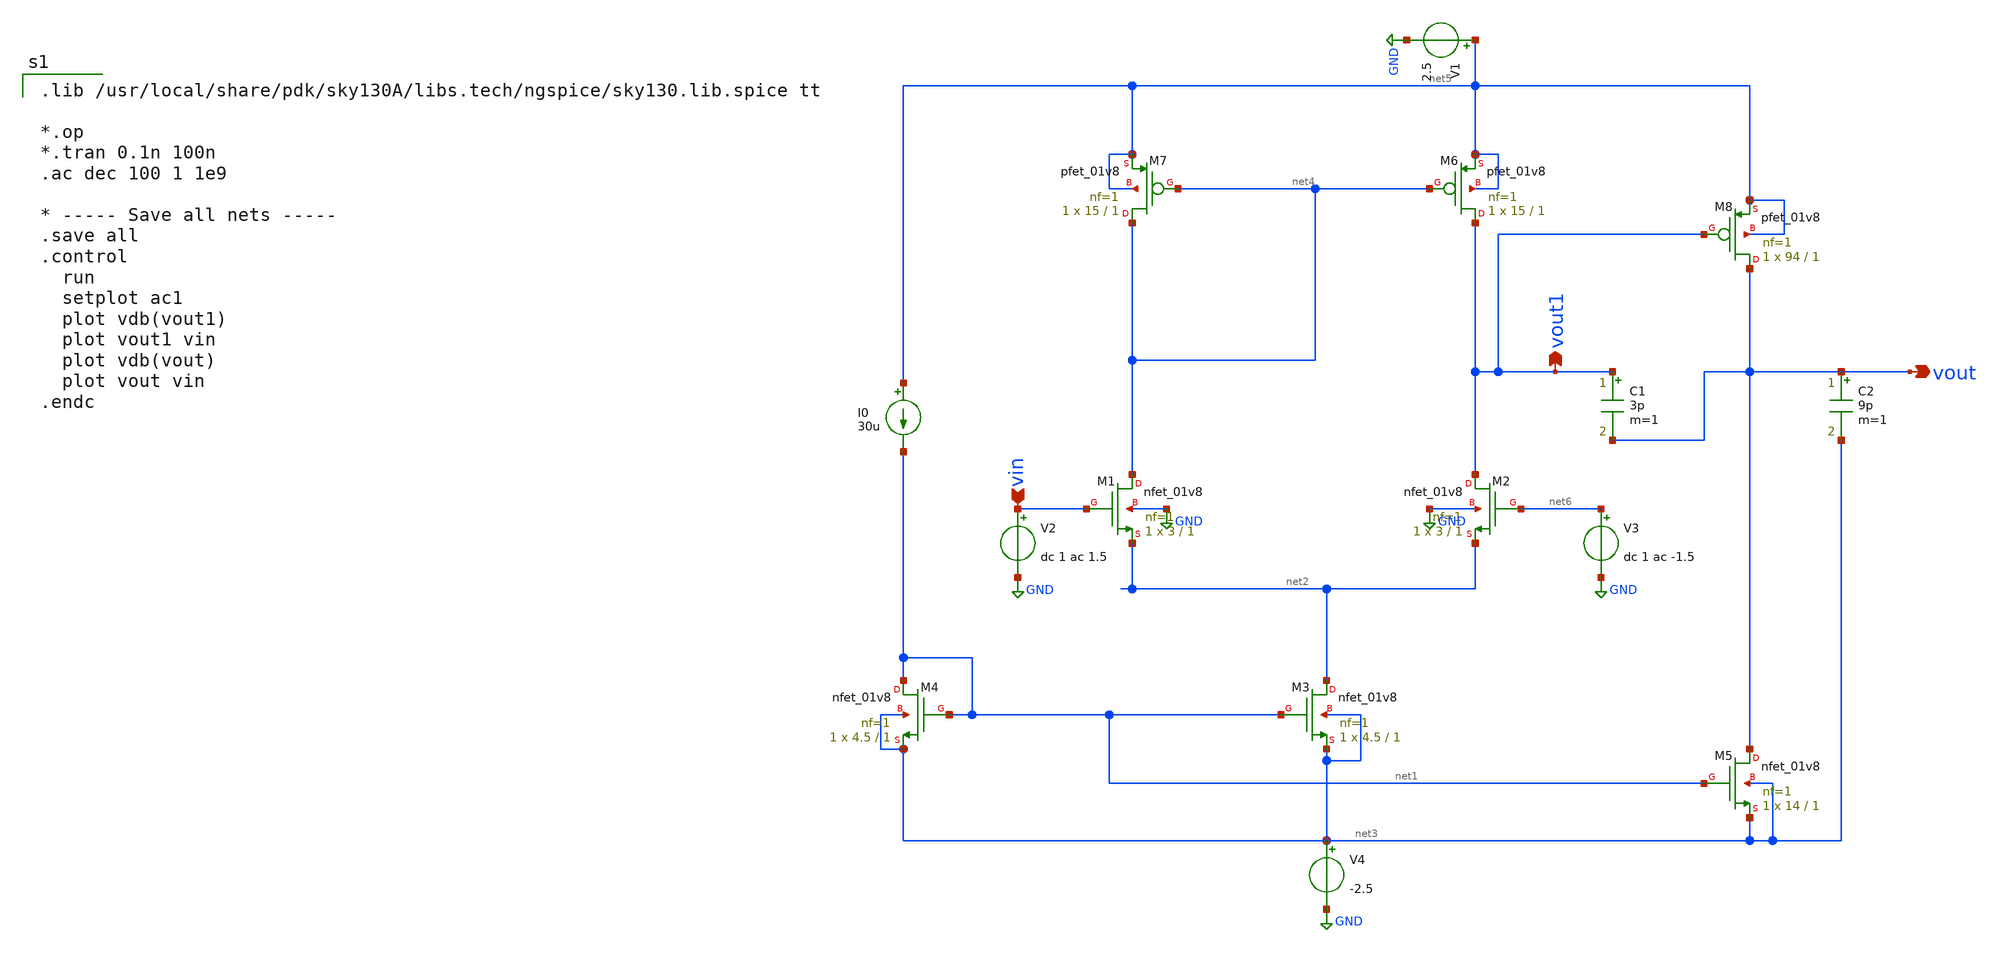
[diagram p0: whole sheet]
** sch_path: 11T_2stage.sch
**.subckt 11T_2stage vout vin vout1
*.opin vout
*.ipin vin
*.opin vout1
XM1 net4 vin net2 GND sky130_fd_pr__nfet_01v8 L=1 W=3 nf=1 ad='int((1 + 1)/2) * 3 / 1 * 0.29' as='int((1 + 2)/2) * 3 / 1 * 0.29'
+ pd='2*int((1 + 1)/2) * (3 / 1 + 0.29)' ps='2*int((1 + 2)/2) * (3 / 1 + 0.29)' nrd='0.29 / 3 ' nrs='0.29 / 3 '
+ sa=0 sb=0 sd=0 mult=1 m=1
XM2 vout1 net6 net2 GND sky130_fd_pr__nfet_01v8 L=1 W=3 nf=1 ad='int((1 + 1)/2) * 3 / 1 * 0.29' as='int((1 + 2)/2) * 3 / 1 * 0.29'
+ pd='2*int((1 + 1)/2) * (3 / 1 + 0.29)' ps='2*int((1 + 2)/2) * (3 / 1 + 0.29)' nrd='0.29 / 3 ' nrs='0.29 / 3 '
+ sa=0 sb=0 sd=0 mult=1 m=1
XM3 net2 net1 net3 net3 sky130_fd_pr__nfet_01v8 L=1 W=4.5 nf=1 ad='int((1 + 1)/2) * 4.5 / 1 * 0.29' as='int((1 + 2)/2) * 4.5 / 1 * 0.29'
+ pd='2*int((1 + 1)/2) * (4.5 / 1 + 0.29)' ps='2*int((1 + 2)/2) * (4.5 / 1 + 0.29)' nrd='0.29 / 4.5 ' nrs='0.29 / 4.5 '
+ sa=0 sb=0 sd=0 mult=1 m=1
XM4 net1 net1 net3 net3 sky130_fd_pr__nfet_01v8 L=1 W=4.5 nf=1 ad='int((1 + 1)/2) * 4.5 / 1 * 0.29' as='int((1 + 2)/2) * 4.5 / 1 * 0.29'
+ pd='2*int((1 + 1)/2) * (4.5 / 1 + 0.29)' ps='2*int((1 + 2)/2) * (4.5 / 1 + 0.29)' nrd='0.29 / 4.5 ' nrs='0.29 / 4.5 '
+ sa=0 sb=0 sd=0 mult=1 m=1
XM5 vout net1 net3 net3 sky130_fd_pr__nfet_01v8 L=1 W=14 nf=1 ad='int((1 + 1)/2) * 14 / 1 * 0.29' as='int((1 + 2)/2) * 14 / 1 * 0.29'
+ pd='2*int((1 + 1)/2) * (14 / 1 + 0.29)' ps='2*int((1 + 2)/2) * (14 / 1 + 0.29)' nrd='0.29 / 14 ' nrs='0.29 / 14 '
+ sa=0 sb=0 sd=0 mult=1 m=1
XM6 vout1 net4 net5 net5 sky130_fd_pr__pfet_01v8 L=1 W=15 nf=1 ad='int((1 + 1)/2) * 15 / 1 * 0.29' as='int((1 + 2)/2) * 15 / 1 * 0.29'
+ pd='2*int((1 + 1)/2) * (15 / 1 + 0.29)' ps='2*int((1 + 2)/2) * (15 / 1 + 0.29)' nrd='0.29 / 15 ' nrs='0.29 / 15 '
+ sa=0 sb=0 sd=0 mult=1 m=1
XM7 net4 net4 net5 net5 sky130_fd_pr__pfet_01v8 L=1 W=15 nf=1 ad='int((1 + 1)/2) * 15 / 1 * 0.29' as='int((1 + 2)/2) * 15 / 1 * 0.29'
+ pd='2*int((1 + 1)/2) * (15 / 1 + 0.29)' ps='2*int((1 + 2)/2) * (15 / 1 + 0.29)' nrd='0.29 / 15 ' nrs='0.29 / 15 '
+ sa=0 sb=0 sd=0 mult=1 m=1
XM8 vout vout1 net5 net5 sky130_fd_pr__pfet_01v8 L=1 W=94 nf=1 ad='int((1 + 1)/2) * 94 / 1 * 0.29' as='int((1 + 2)/2) * 94 / 1 * 0.29'
+ pd='2*int((1 + 1)/2) * (94 / 1 + 0.29)' ps='2*int((1 + 2)/2) * (94 / 1 + 0.29)' nrd='0.29 / 94 ' nrs='0.29 / 94 '
+ sa=0 sb=0 sd=0 mult=1 m=1
C1 vout1 vout 3p m=1
V1 net5 GND 2.5
I0 net5 net1 30u
V2 vin GND dc 1 ac 1.5
V3 net6 GND dc 1 ac -1.5
V4 net3 GND -2.5
C2 vout net3 9p m=1
**** begin user architecture code

.lib /usr/local/share/pdk/sky130A/libs.tech/ngspice/sky130.lib.spice tt

*.op
*.tran 0.1n 100n
.ac dec 100 1 1e9

* ----- Save all nets -----
.save all
.control
  run
  setplot ac1
  plot vdb(vout1)
  plot vout1 vin
  plot vdb(vout)
  plot vout vin
.endc

**** end user architecture code
**.ends
.GLOBAL GND
.end
